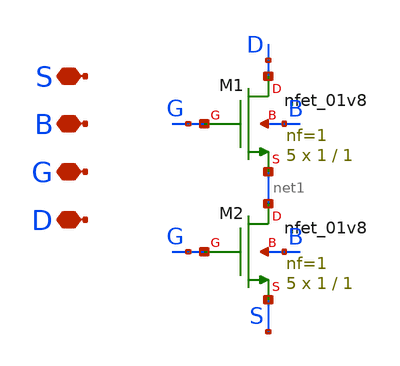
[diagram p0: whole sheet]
** sch_path: xschem/INA/Transistors/transistors_bias_network/nfet_m17m18.sch
**.subckt nfet_m17m18 S B G D
*.iopin S
*.iopin B
*.iopin G
*.iopin D
XM1 D G net1 B sky130_fd_pr__nfet_01v8 L=1 W=1 nf=1 ad='int((nf+1)/2) * W/nf * 0.29' as='int((nf+2)/2) * W/nf * 0.29'
+ pd='2*int((nf+1)/2) * (W/nf + 0.29)' ps='2*int((nf+2)/2) * (W/nf + 0.29)' nrd='0.29 / W' nrs='0.29 / W'
+ sa=0 sb=0 sd=0 mult=5 m=5
XM2 net1 G S B sky130_fd_pr__nfet_01v8 L=1 W=1 nf=1 ad='int((nf+1)/2) * W/nf * 0.29' as='int((nf+2)/2) * W/nf * 0.29'
+ pd='2*int((nf+1)/2) * (W/nf + 0.29)' ps='2*int((nf+2)/2) * (W/nf + 0.29)' nrd='0.29 / W' nrs='0.29 / W'
+ sa=0 sb=0 sd=0 mult=5 m=5
**.ends
.end
